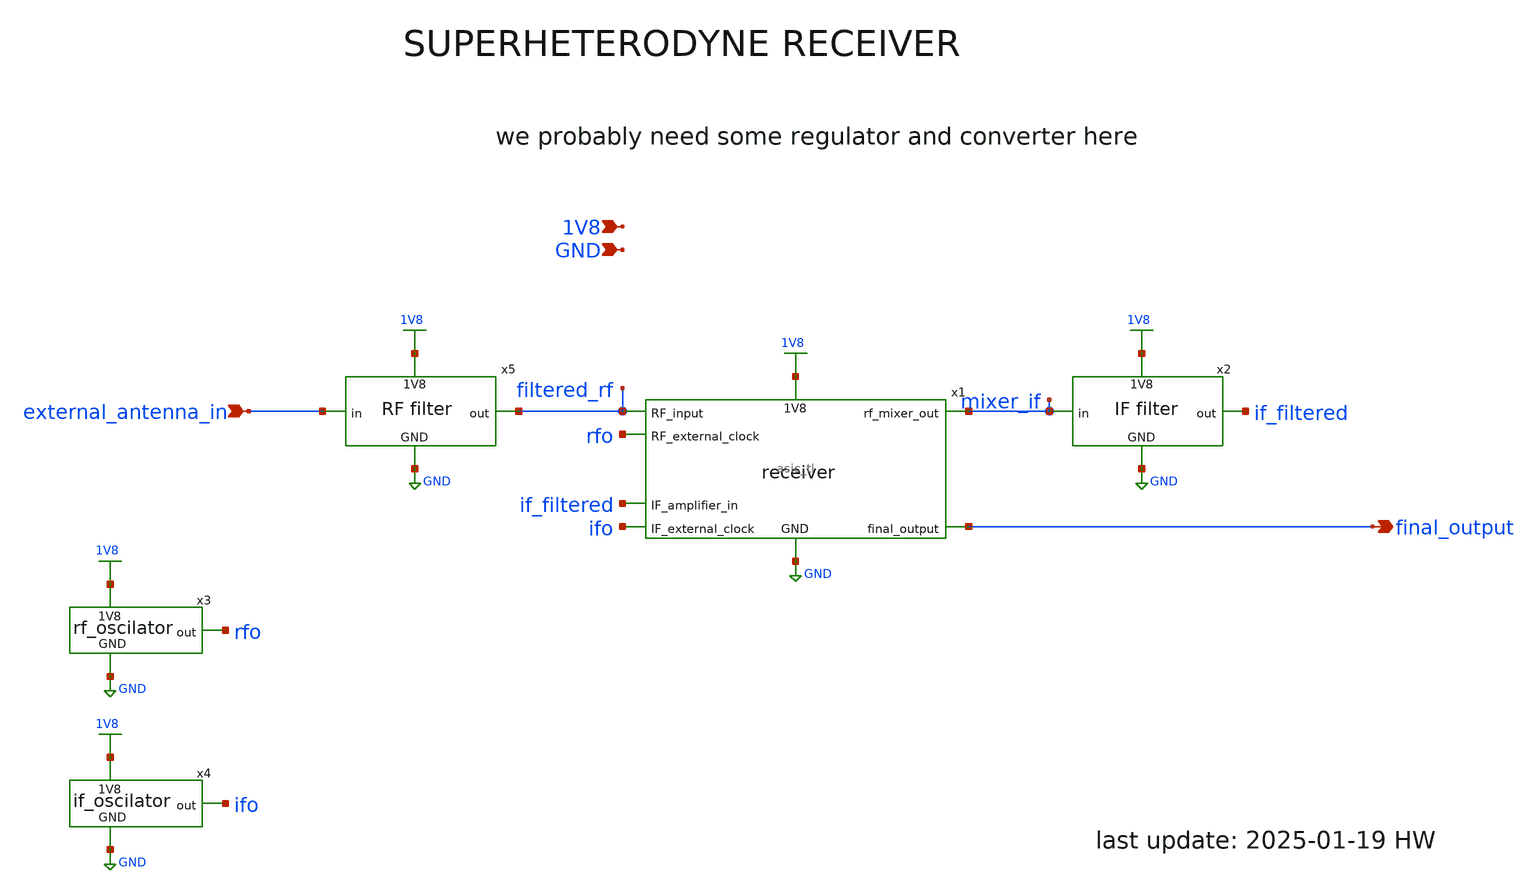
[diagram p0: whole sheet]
** sch_path: schematic/top_level.sch
**.subckt top_level 1V8 GND external_antenna_in final_output
*.ipin 1V8
*.ipin GND
*.ipin external_antenna_in
*.opin final_output
x1 1V8 GND mixer_if filtered_rf rfo final_output ifo if_filtered asic_tl
x2 1V8 mixer_if if_filtered GND if_filter
x3 1V8 rfo GND rf_oscilator
x4 1V8 ifo GND if_oscilator
x5 1V8 external_antenna_in filtered_rf GND rf_filter
**.ends
.GLOBAL 1V8
.GLOBAL GND
.end
